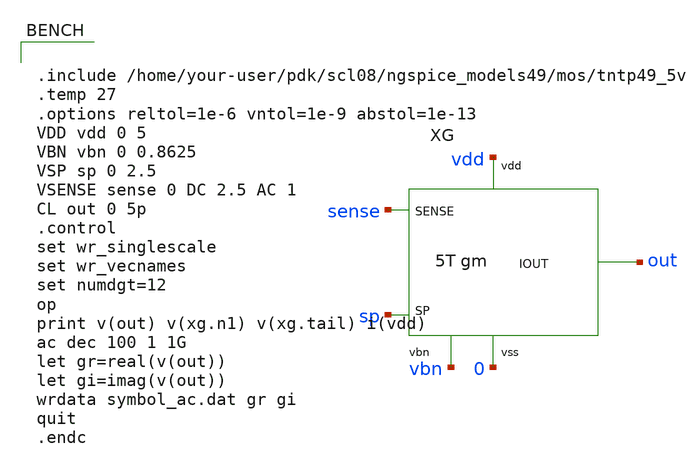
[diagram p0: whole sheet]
** sch_path: OTA/design_review/gm_ota_vbn_0p8625/tb/gm_ota_symbol_tb.sch
**.subckt gm_ota_symbol_tb
XG sense sp vdd 0 vbn out gm_ota
**** begin user architecture code


.include /home/your-user/pdk/scl08/ngspice_models49/mos/tntp49_5v
.temp 27
.options reltol=1e-6 vntol=1e-9 abstol=1e-13
VDD vdd 0 5
VBN vbn 0 0.8625
VSP sp 0 2.5
VSENSE sense 0 DC 2.5 AC 1
CL out 0 5p
.control
set wr_singlescale
set wr_vecnames
set numdgt=12
op
print v(out) v(xg.n1) v(xg.tail) i(vdd)
ac dec 100 1 1G
let gr=real(v(out))
let gi=imag(v(out))
wrdata symbol_ac.dat gr gi
quit
.endc


**** end user architecture code
**.ends
.end
